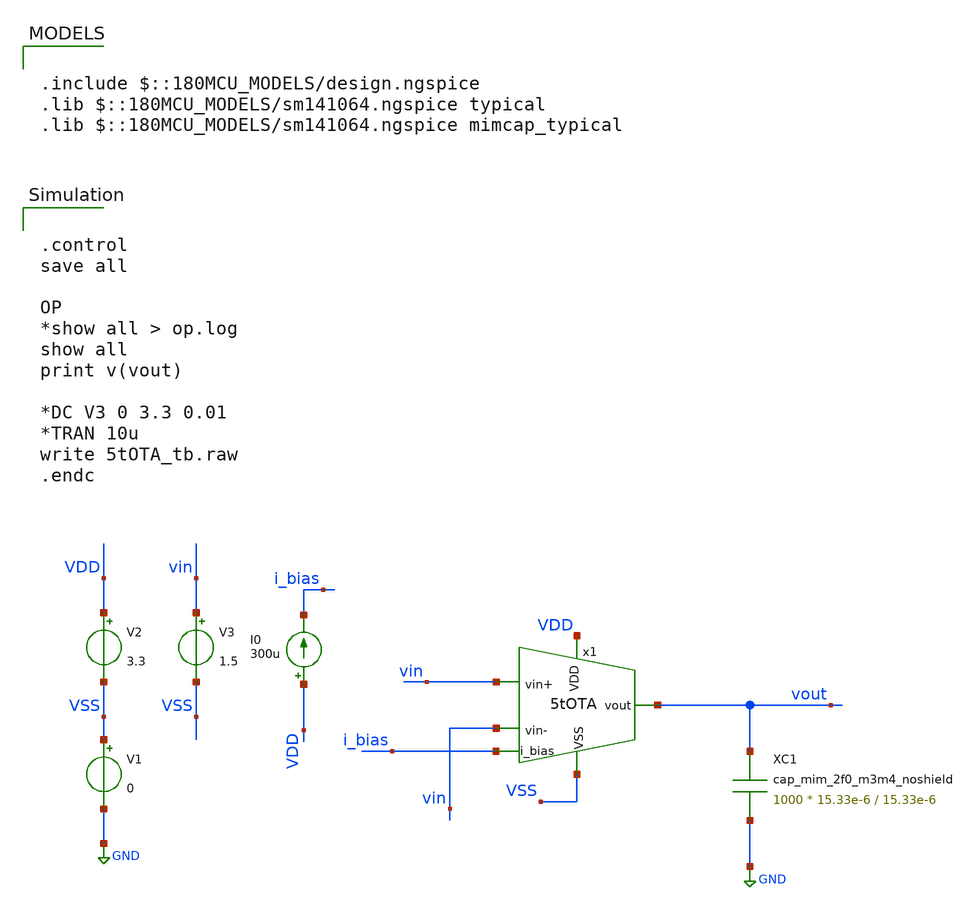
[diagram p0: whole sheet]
** sch_path: designs/5tOTA_tb.sch
**.subckt 5tOTA_tb
x1 VDD vout vin vin i_bias VSS 5tOTA
V1 VSS GND 0
V2 VDD VSS 3.3
I0 VDD i_bias 300u
V3 vin VSS 1.5
XC1 vout GND cap_mim_2f0_m3m4_noshield c_width=15.33e-6 c_length=15.33e-6 m=1000
**** begin user architecture code

.include $::180MCU_MODELS/design.ngspice
.lib $::180MCU_MODELS/sm141064.ngspice typical
.lib $::180MCU_MODELS/sm141064.ngspice mimcap_typical



.control
save all

OP
*show all > op.log
show all
print v(vout)

*DC V3 0 3.3 0.01
*TRAN 10u
write 5tOTA_tb.raw
.endc


**** end user architecture code
**.ends

* expanding   symbol:  5tOTA.sym # of pins=6
** sym_path: designs/5tOTA.sym
** sch_path: designs/5tOTA.sch
.subckt 5tOTA VDD vout vin+ vin- i_bias VSS
*.ipin VDD
*.opin vout
*.ipin i_bias
*.ipin vin+
*.ipin vin-
*.ipin VSS
XM1 net1 vin+ net2 VSS nfet_03v3 L=0.5u W=11.43u nf=1 ad='int((nf+1)/2) * W/nf * 0.18u' as='int((nf+2)/2) * W/nf * 0.18u'
+ pd='2*int((nf+1)/2) * (W/nf + 0.18u)' ps='2*int((nf+2)/2) * (W/nf + 0.18u)' nrd='0.18u / W' nrs='0.18u / W'
+ sa=0 sb=0 sd=0 m=1
XM2 vout vin- net2 VSS nfet_03v3 L=0.5u W=11.43u nf=1 ad='int((nf+1)/2) * W/nf * 0.18u' as='int((nf+2)/2) * W/nf * 0.18u'
+ pd='2*int((nf+1)/2) * (W/nf + 0.18u)' ps='2*int((nf+2)/2) * (W/nf + 0.18u)' nrd='0.18u / W' nrs='0.18u / W'
+ sa=0 sb=0 sd=0 m=1
XM3 net1 net1 VDD VDD pfet_03v3 L=0.5u W=22.86u nf=1 ad='int((nf+1)/2) * W/nf * 0.18u' as='int((nf+2)/2) * W/nf * 0.18u'
+ pd='2*int((nf+1)/2) * (W/nf + 0.18u)' ps='2*int((nf+2)/2) * (W/nf + 0.18u)' nrd='0.18u / W' nrs='0.18u / W'
+ sa=0 sb=0 sd=0 m=1
XM4 vout net1 VDD VDD pfet_03v3 L=0.5u W=22.86u nf=1 ad='int((nf+1)/2) * W/nf * 0.18u' as='int((nf+2)/2) * W/nf * 0.18u'
+ pd='2*int((nf+1)/2) * (W/nf + 0.18u)' ps='2*int((nf+2)/2) * (W/nf + 0.18u)' nrd='0.18u / W' nrs='0.18u / W'
+ sa=0 sb=0 sd=0 m=1
XM5 net2 i_bias VSS VSS nfet_03v3 L=0.5u W=22.86u nf=1 ad='int((nf+1)/2) * W/nf * 0.18u' as='int((nf+2)/2) * W/nf * 0.18u'
+ pd='2*int((nf+1)/2) * (W/nf + 0.18u)' ps='2*int((nf+2)/2) * (W/nf + 0.18u)' nrd='0.18u / W' nrs='0.18u / W'
+ sa=0 sb=0 sd=0 m=1
XM6 i_bias i_bias VSS VSS nfet_03v3 L=0.5u W=22.86u nf=1 ad='int((nf+1)/2) * W/nf * 0.18u' as='int((nf+2)/2) * W/nf * 0.18u'
+ pd='2*int((nf+1)/2) * (W/nf + 0.18u)' ps='2*int((nf+2)/2) * (W/nf + 0.18u)' nrd='0.18u / W' nrs='0.18u / W'
+ sa=0 sb=0 sd=0 m=1
.ends

.GLOBAL GND
.end
